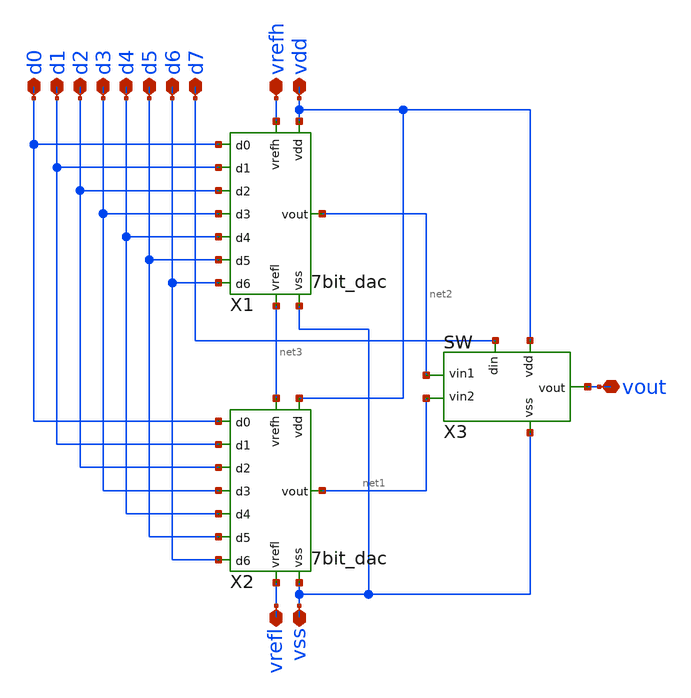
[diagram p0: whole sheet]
** sch_path: dac5v/1.schematics/8bit_dac.sch
**.subckt 8bit_dac vdd vss vrefh vrefl d0 d1 d2 d3 d4 d5 d6 d7 vout
*.iopin vdd
*.iopin vss
*.iopin vrefh
*.iopin vrefl
*.iopin d0
*.iopin d1
*.iopin d2
*.iopin d3
*.iopin d4
*.iopin d5
*.iopin d6
*.iopin d7
*.iopin vout
X1 vdd vss vrefh net3 d0 d1 d2 d3 d4 d5 d6 net2 7bit_dac
X2 vdd vss net3 vrefl d0 d1 d2 d3 d4 d5 d6 net1 7bit_dac
X3 vdd vss d7 net2 net1 vout sw
**.ends
.end
